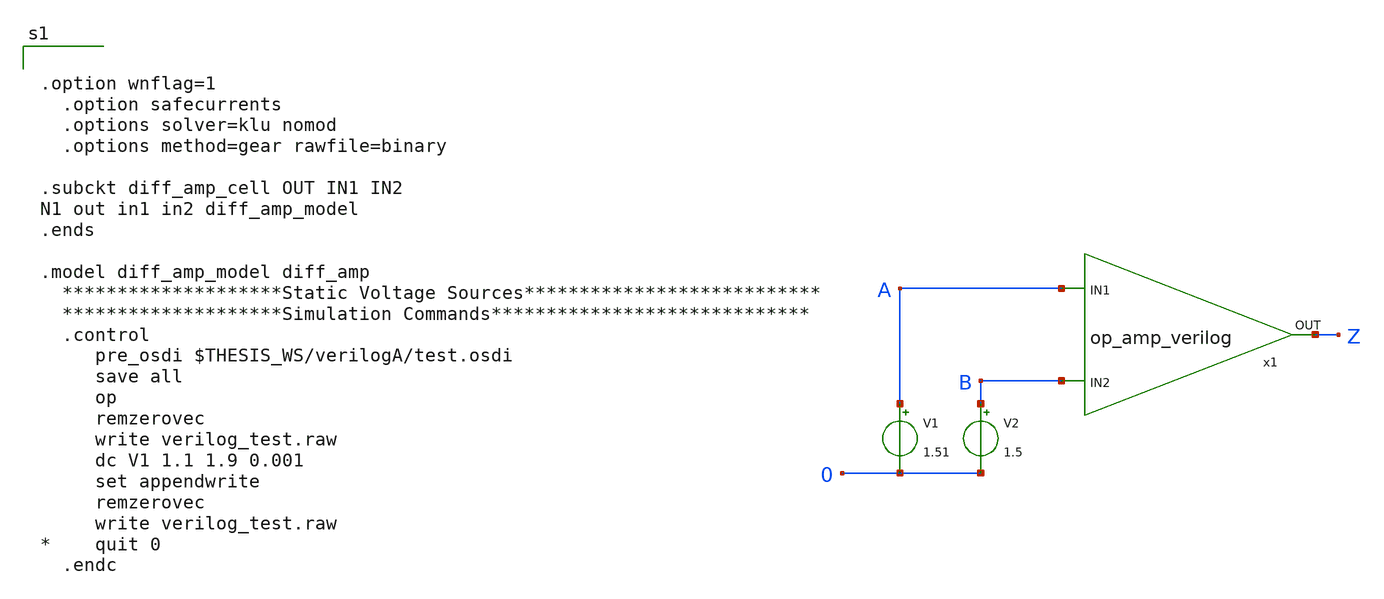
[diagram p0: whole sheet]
** sch_path: xschem/verilogA_test.sch
**.subckt verilogA_test
x1 Z A B diff_amp_cell
V1 A 0 1.51
V2 B 0 1.5
**** begin user architecture code


.option wnflag=1
  .option safecurrents
  .options solver=klu nomod
  .options method=gear rawfile=binary

.subckt diff_amp_cell OUT IN1 IN2
N1 out in1 in2 diff_amp_model
.ends

.model diff_amp_model diff_amp
  ********************Static Voltage Sources***************************
  ********************Simulation Commands*****************************
  .control
     pre_osdi $THESIS_WS/verilogA/test.osdi
     save all
     op
     remzerovec
     write verilog_test.raw
     dc V1 1.1 1.9 0.001
     set appendwrite
     remzerovec
     write verilog_test.raw
*    quit 0
  .endc


**** end user architecture code
**.ends
.end
